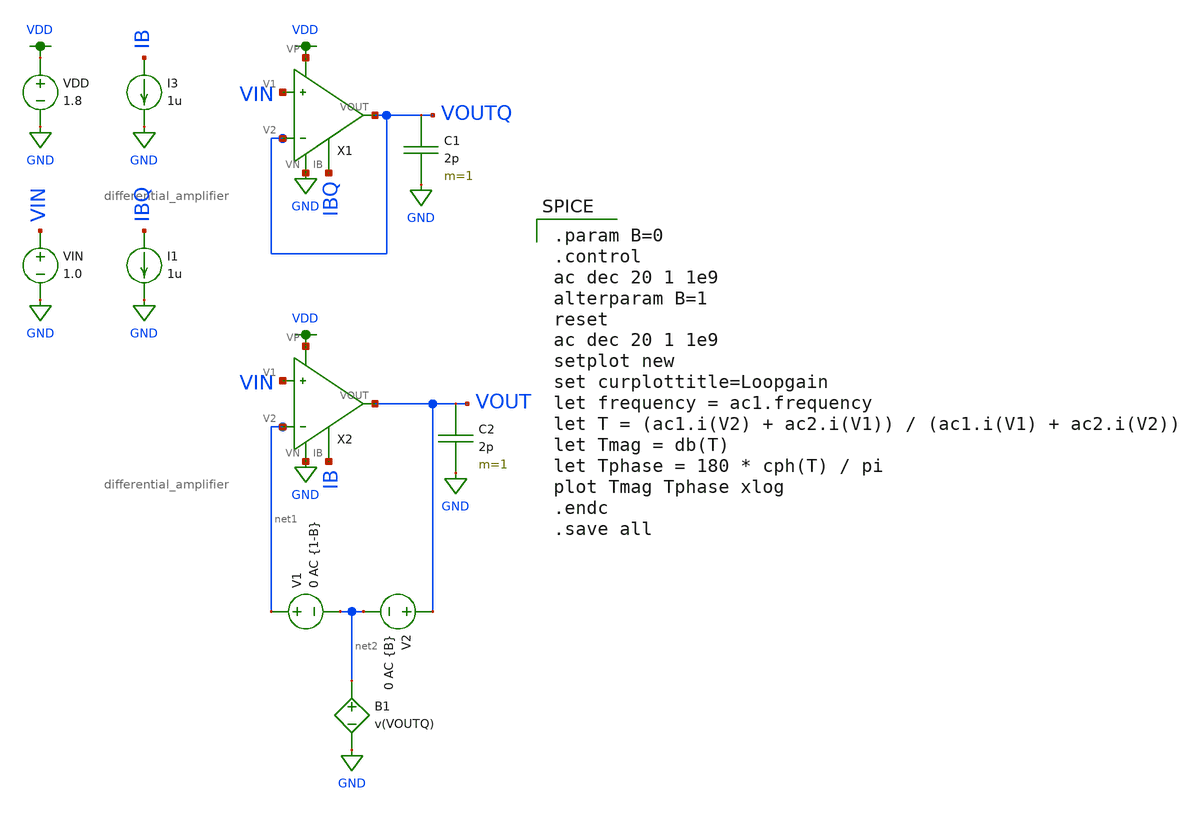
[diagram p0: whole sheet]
** sch_path: differential_amplifier/schematics/differential_amplifier_tran_c.sch
**.subckt differential_amplifier_tran_c
VDD VDD GND 1.8
VIN VIN GND 1.0
C1 VOUTQ GND 2p m=1
C2 VOUT GND 2p m=1
V1 net1 net2 0 AC {1-B}
V2 VOUT net2 0 AC {B}
B1 net2 GND V=v(VOUTQ)
X2 VIN net1 VDD GND IB VOUT differential_amplifier
X1 VIN VOUTQ VDD GND IBQ VOUTQ differential_amplifier
I3 IB GND 1u
I1 IBQ GND 1u
**** begin user architecture code

.option wnflag=1
.lib ~/skywater/skywater-pdk/libraries/sky130_fd_pr_ngspice/latest/models/sky130.lib.spice tt


.param B=0
.control
ac dec 20 1 1e9
alterparam B=1
reset
ac dec 20 1 1e9
setplot new
set curplottitle=Loopgain
let frequency = ac1.frequency
let T = (ac1.i(V2) + ac2.i(V1)) / (ac1.i(V1) + ac2.i(V2))
let Tmag = db(T)
let Tphase = 180 * cph(T) / pi
plot Tmag Tphase xlog
.endc
.save all

**** end user architecture code
**.ends
.GLOBAL GND
.GLOBAL VDD
.end
